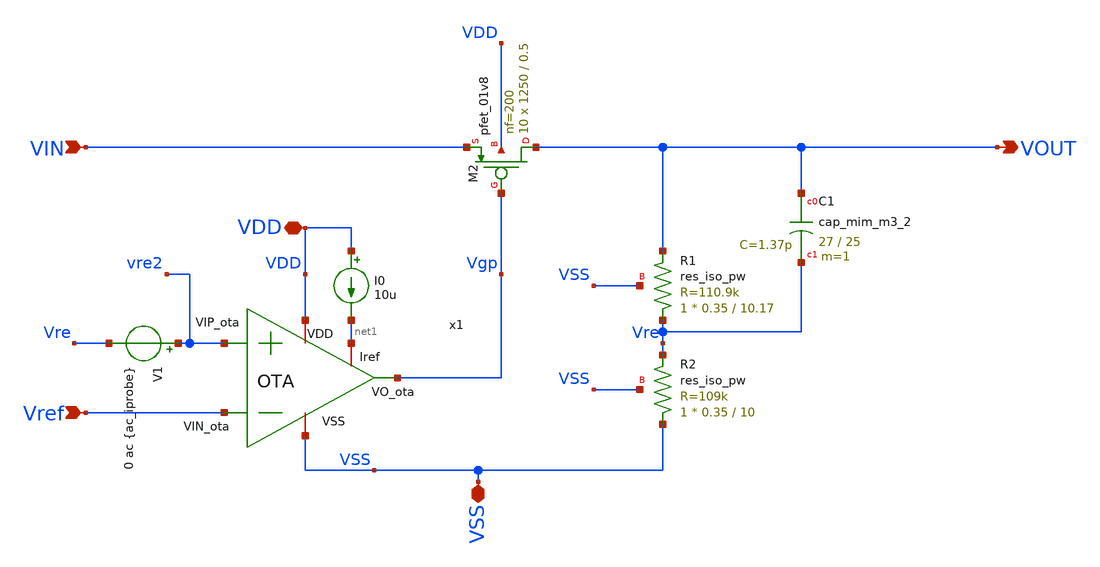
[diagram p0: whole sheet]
** sch_path: xschem/LDO.sch
**.subckt LDO VIN VDD VOUT Vref VSS
*.ipin VIN
*.iopin VDD
*.opin VOUT
*.ipin Vref
*.iopin VSS
XR1 Vre VOUT VSS sky130_fd_pr__res_iso_pw W=0.35 L=10.17 m=1
XR2 VSS Vre VSS sky130_fd_pr__res_iso_pw W=0.35 L=10 m=1
V1 vre2 Vre 0 ac {ac_iprobe}
x1 VDD Vgp Vref vre2 VSS net1 OTA
XM2 VOUT Vgp VIN VDD sky130_fd_pr__pfet_01v8 L=0.5 W=1250 nf=200 ad='int((200 + 1)/2) * 1250 / 200 * 0.29'
+ as='int((200 + 2)/2) * 1250 / 200 * 0.29' pd='2*int((200 + 1)/2) * (1250 / 200 + 0.29)' ps='2*int((200 + 2)/2) * (1250 / 200 + 0.29)'
+ nrd='0.29 / 1250 ' nrs='0.29 / 1250 ' sa=0 sb=0 sd=0 mult=10 m=10
XC1 VOUT Vre sky130_fd_pr__cap_mim_m3_2 W=27 L=25 MF=1 m=1
I0 VDD net1 10u
**.ends

* expanding   symbol:  /foss/designs/LDO-sky130/xschem/OTA.sym # of pins=6
** sym_path: xschem/OTA.sym
** sch_path: xschem/OTA.sch
.subckt OTA VDD VO_ota VIN_ota VIP_ota VSS Iref
*.ipin VIN_ota
*.opin VO_ota
*.iopin VSS
*.iopin VDD
*.ipin VIP_ota
*.iopin Iref
XMpr VO_ota1 vd VSS VSS sky130_fd_pr__nfet_01v8 L=0.5 W=3 nf=1 ad='int((1 + 1)/2) * 3 / 1 * 0.29' as='int((1 + 2)/2) * 3 / 1 * 0.29'
+ pd='2*int((1 + 1)/2) * (3 / 1 + 0.29)' ps='2*int((1 + 2)/2) * (3 / 1 + 0.29)' nrd='0.29 / 3 ' nrs='0.29 / 3 '
+ sa=0 sb=0 sd=0 mult=1 m=1
XMnr vd vd VSS VSS sky130_fd_pr__nfet_01v8 L=0.5 W=3 nf=1 ad='int((1 + 1)/2) * 3 / 1 * 0.29' as='int((1 + 2)/2) * 3 / 1 * 0.29'
+ pd='2*int((1 + 1)/2) * (3 / 1 + 0.29)' ps='2*int((1 + 2)/2) * (3 / 1 + 0.29)' nrd='0.29 / 3 ' nrs='0.29 / 3 '
+ sa=0 sb=0 sd=0 mult=1 m=1
XMn vd VIN_ota Vtail VDD sky130_fd_pr__pfet_01v8 L=0.5 W=28 nf=1 ad='int((1 + 1)/2) * 28 / 1 * 0.29'
+ as='int((1 + 2)/2) * 28 / 1 * 0.29' pd='2*int((1 + 1)/2) * (28 / 1 + 0.29)' ps='2*int((1 + 2)/2) * (28 / 1 + 0.29)'
+ nrd='0.29 / 28 ' nrs='0.29 / 28 ' sa=0 sb=0 sd=0 mult=1 m=1
XMp VO_ota1 VIP_ota Vtail VDD sky130_fd_pr__pfet_01v8 L=0.5 W=28 nf=1 ad='int((1 + 1)/2) * 28 / 1 * 0.29'
+ as='int((1 + 2)/2) * 28 / 1 * 0.29' pd='2*int((1 + 1)/2) * (28 / 1 + 0.29)' ps='2*int((1 + 2)/2) * (28 / 1 + 0.29)'
+ nrd='0.29 / 28 ' nrs='0.29 / 28 ' sa=0 sb=0 sd=0 mult=1 m=1
XMo VO_ota VO_ota1 VSS VSS sky130_fd_pr__nfet_01v8 L=0.5 W=3 nf=1 ad='int((1 + 1)/2) * 3 / 1 * 0.29'
+ as='int((1 + 2)/2) * 3 / 1 * 0.29' pd='2*int((1 + 1)/2) * (3 / 1 + 0.29)' ps='2*int((1 + 2)/2) * (3 / 1 + 0.29)'
+ nrd='0.29 / 3 ' nrs='0.29 / 3 ' sa=0 sb=0 sd=0 mult=1 m=1
XMc3 VGP Iref VSS VSS sky130_fd_pr__nfet_01v8 L=0.5 W=1 nf=1 ad='int((1 + 1)/2) * 1 / 1 * 0.29' as='int((1 + 2)/2) * 1 / 1 * 0.29'
+ pd='2*int((1 + 1)/2) * (1 / 1 + 0.29)' ps='2*int((1 + 2)/2) * (1 / 1 + 0.29)' nrd='0.29 / 1 ' nrs='0.29 / 1 '
+ sa=0 sb=0 sd=0 mult=1 m=1
XMp2 Iref Iref VSS VSS sky130_fd_pr__nfet_01v8 L=0.5 W=1 nf=1 ad='int((1 + 1)/2) * 1 / 1 * 0.29' as='int((1 + 2)/2) * 1 / 1 * 0.29'
+ pd='2*int((1 + 1)/2) * (1 / 1 + 0.29)' ps='2*int((1 + 2)/2) * (1 / 1 + 0.29)' nrd='0.29 / 1 ' nrs='0.29 / 1 '
+ sa=0 sb=0 sd=0 mult=1 m=1
XMr VGP VGP VDD VDD sky130_fd_pr__pfet_01v8_lvt L=0.5 W=2.4 nf=1 ad='int((1 + 1)/2) * 2.4 / 1 * 0.29'
+ as='int((1 + 2)/2) * 2.4 / 1 * 0.29' pd='2*int((1 + 1)/2) * (2.4 / 1 + 0.29)' ps='2*int((1 + 2)/2) * (2.4 / 1 + 0.29)'
+ nrd='0.29 / 2.4 ' nrs='0.29 / 2.4 ' sa=0 sb=0 sd=0 mult=1 m=1
XMrc1 Vtail VGP VDD VDD sky130_fd_pr__pfet_01v8_lvt L=0.5 W=19.4 nf=1 ad='int((1 + 1)/2) * 19.4 / 1 * 0.29'
+ as='int((1 + 2)/2) * 19.4 / 1 * 0.29' pd='2*int((1 + 1)/2) * (19.4 / 1 + 0.29)' ps='2*int((1 + 2)/2) * (19.4 / 1 + 0.29)'
+ nrd='0.29 / 19.4 ' nrs='0.29 / 19.4 ' sa=0 sb=0 sd=0 mult=1 m=1
XMrc2 VO_ota VGP VDD VDD sky130_fd_pr__pfet_01v8_lvt L=0.5 W=8 nf=1 ad='int((1 + 1)/2) * 8 / 1 * 0.29'
+ as='int((1 + 2)/2) * 8 / 1 * 0.29' pd='2*int((1 + 1)/2) * (8 / 1 + 0.29)' ps='2*int((1 + 2)/2) * (8 / 1 + 0.29)'
+ nrd='0.29 / 8 ' nrs='0.29 / 8 ' sa=0 sb=0 sd=0 mult=1 m=1
XR1 VO_ota1 net1 VSS sky130_fd_pr__res_high_po W=0.35 L=250 mult=1 m=1
XC1 VO_ota net1 sky130_fd_pr__cap_mim_m3_2 W=10 L=50 MF=10 m=10
.ends

.end
